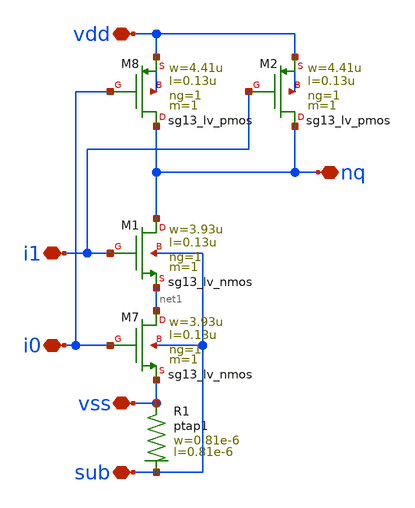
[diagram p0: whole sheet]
** sch_path: MSPHY6034-main/dependencies/unic_cass_2025_team04_padring/xschem/openpdk-libraries/ihp-sg13g2/sg13g2_io/xschem/sg13g2_io_nand2_x1.sch
**.subckt sg13g2_io_nand2_x1 vss nq i0 vdd sub i1
*.iopin vss
*.iopin nq
*.iopin i0
*.iopin vdd
*.iopin sub
*.iopin i1
XR1 vss sub ptap1 R=251.5 w=0.81e-6 l=0.81e-6
XM7 net1 i0 vss sub sg13_lv_nmos w=3.93u l=0.13u ng=1 m=1 mm_ok=1
XM8 nq i0 vdd vdd sg13_lv_pmos w=4.41u l=0.13u ng=1 m=1 mm_ok=1
XM2 nq i1 vdd vdd sg13_lv_pmos w=4.41u l=0.13u ng=1 m=1 mm_ok=1
XM1 nq i1 net1 sub sg13_lv_nmos w=3.93u l=0.13u ng=1 m=1 mm_ok=1
**.ends
.end
